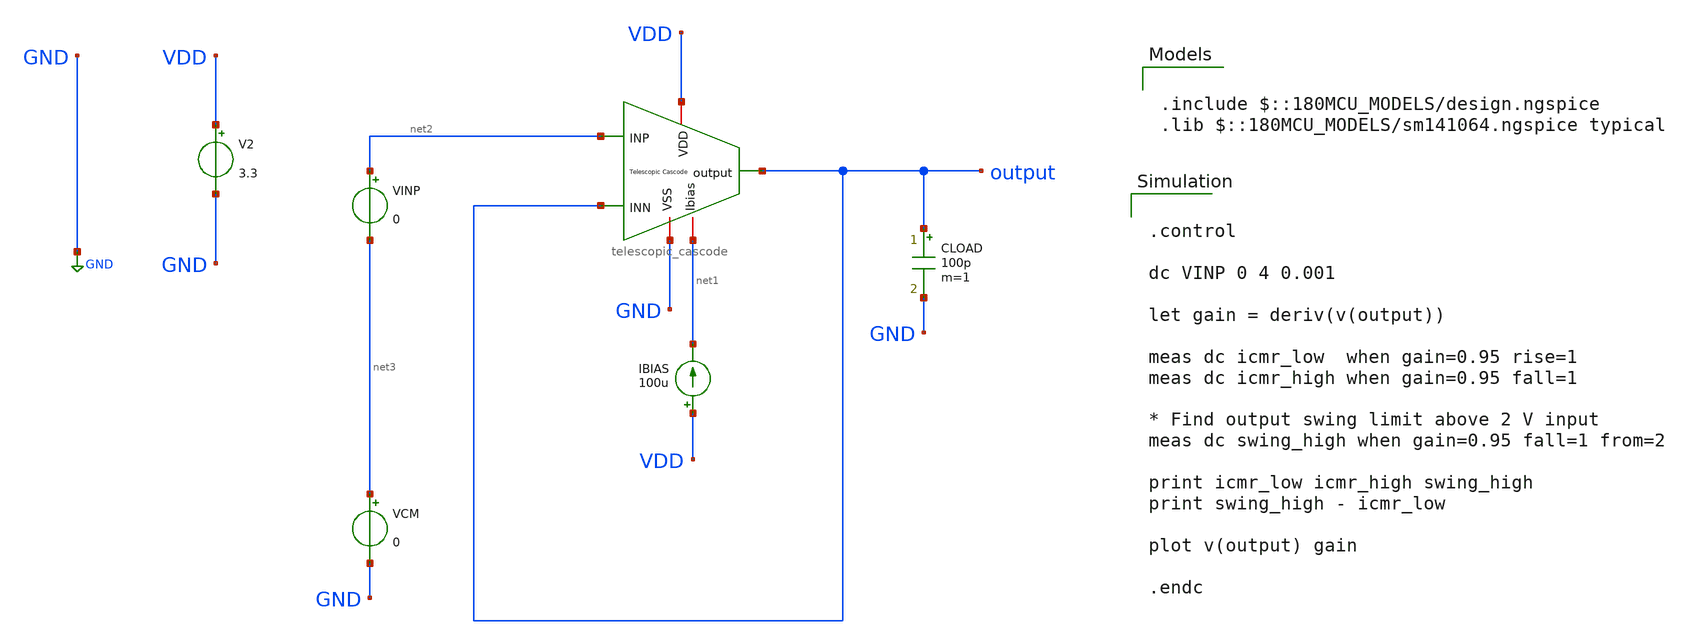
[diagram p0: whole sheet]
** sch_path: designs/libs/core_amps/ota_telescopic/tb/telescopic_dc_unity.sch
**.subckt telescopic_dc_unity
IBIAS VDD net1 100u
V2 VDD GND 3.3
CLOAD output GND 100p m=1
VINP net2 net3 0
VCM net3 GND 0
x1 VDD output output net2 GND net1 telescopic_cascode
**** begin user architecture code

.include $::180MCU_MODELS/design.ngspice
.lib $::180MCU_MODELS/sm141064.ngspice typical



.control

dc VINP 0 4 0.001

let gain = deriv(v(output))

meas dc icmr_low  when gain=0.95 rise=1
meas dc icmr_high when gain=0.95 fall=1

* Find output swing limit above 2 V input
meas dc swing_high when gain=0.95 fall=1 from=2

print icmr_low icmr_high swing_high
print swing_high - icmr_low

plot v(output) gain

.endc


**** end user architecture code
**.ends
.GLOBAL GND
.end
